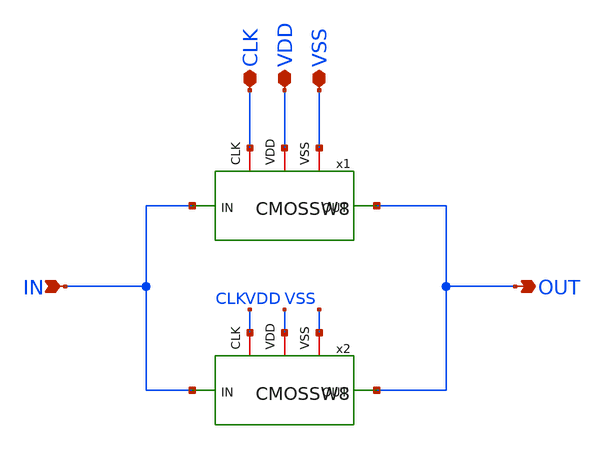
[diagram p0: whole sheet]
** sch_path: CMOSSW16.sch
**.subckt CMOSSW16 IN OUT VSS CLK VDD
*.ipin IN
*.opin OUT
*.iopin VSS
*.iopin CLK
*.iopin VDD
x1 CLK VSS OUT IN VDD CMOSSW8
x2 CLK VSS OUT IN VDD CMOSSW8
**.ends
.end
